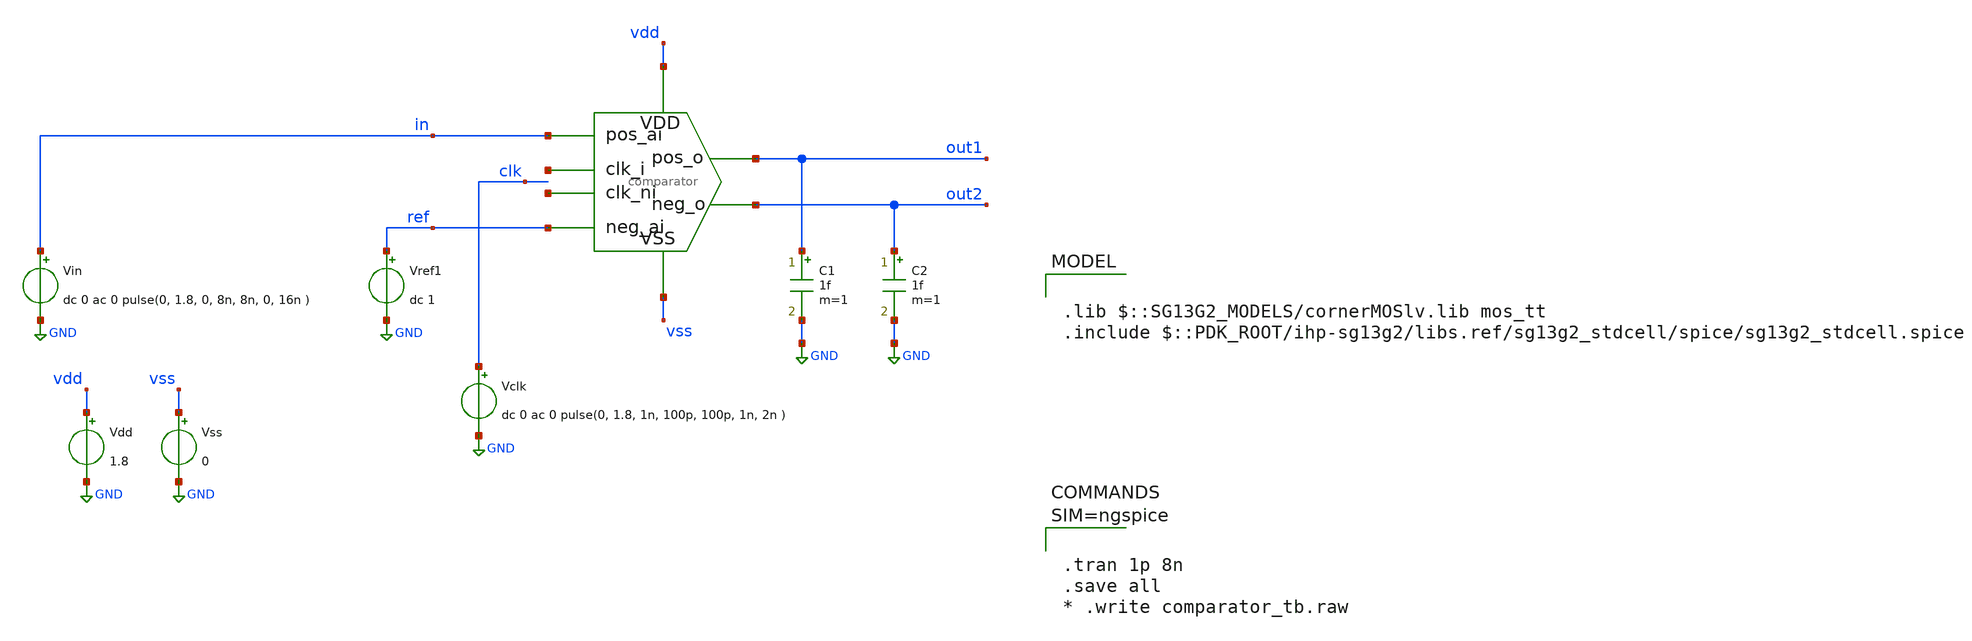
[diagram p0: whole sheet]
** sch_path: designs/comparator/comparator_tb.sch
**.subckt comparator_tb
x1 net1 in ref out2 out1 vss vdd net2 comparator
Vdd vdd GND 1.8
Vss vss GND 0
Vclk clk GND dc 0 ac 0 pulse(0, 1.8, 1n, 100p, 100p, 1n, 2n )
Vin in GND dc 0 ac 0 pulse(0, 1.8, 0, 8n, 8n, 0, 16n )
C1 out1 GND 1f m=1
C2 out2 GND 1f m=1
Vref1 ref GND dc 1
**** begin user architecture code

.lib $::SG13G2_MODELS/cornerMOSlv.lib mos_tt
.include $::PDK_ROOT/ihp-sg13g2/libs.ref/sg13g2_stdcell/spice/sg13g2_stdcell.spice




.tran 1p 8n
.save all
* .write comparator_tb.raw



**** end user architecture code
**.ends

* expanding   symbol:  comparator.sym # of pins=8
** sym_path: designs/comparator_dt/comparator.sym
** sch_path: designs/comparator_dt/comparator.sch
.subckt comparator clk_i pos_ai neg_ai neg_o pos_o VSS VDD clk_ni
*.ipin pos_ai
*.ipin neg_ai
*.ipin VSS
*.ipin VDD
*.opin neg_o
*.opin pos_o
*.ipin clk_i
*.ipin clk_ni
XM12 neg_buf clk_i VDD VDD sg13_lv_pmos w=1.0u l=0.13u ng=1 m=1 mm_ok=1
XM13 pos_buf clk_i VDD VDD sg13_lv_pmos w=1.0u l=0.13u ng=1 m=1 mm_ok=1
XM14 net1 pos_ai neg_buf VSS sg13_lv_nmos w=1.0u l=0.13u ng=1 m=1 mm_ok=1
XM15 net1 neg_ai pos_buf VSS sg13_lv_nmos w=1.0u l=0.13u ng=1 m=1 mm_ok=1
XM16 VSS clk_i net1 VSS sg13_lv_nmos w=1.0u l=0.13u ng=1 m=1 mm_ok=1
XM17 net2 clk_ni VDD VDD sg13_lv_pmos w=2.0u l=0.13u ng=2 m=1 mm_ok=1
XM18 pos_o neg_o net2 VDD sg13_lv_pmos w=2.0u l=0.13u ng=2 m=1 mm_ok=1
XM19 neg_o pos_o net2 VDD sg13_lv_pmos w=2.0u l=0.13u ng=2 m=1 mm_ok=1
XM20 VSS neg_buf pos_o VSS sg13_lv_nmos w=1.0u l=0.13u ng=1 m=1 mm_ok=1
XM21 VSS neg_o pos_o VSS sg13_lv_nmos w=1.0u l=0.13u ng=1 m=1 mm_ok=1
XM22 VSS pos_o neg_o VSS sg13_lv_nmos w=1.0u l=0.13u ng=1 m=1 mm_ok=1
XM23 VSS pos_buf neg_o VSS sg13_lv_nmos w=1.0u l=0.13u ng=1 m=1 mm_ok=1
XC1 neg_buf VSS cap_cmim w=1.41e-5 l=1.41e-5 m=1 mm_ok=1
XC2 pos_buf VSS cap_cmim w=1.41e-5 l=1.41e-5 m=1 mm_ok=1
.ends

.GLOBAL GND
.end
